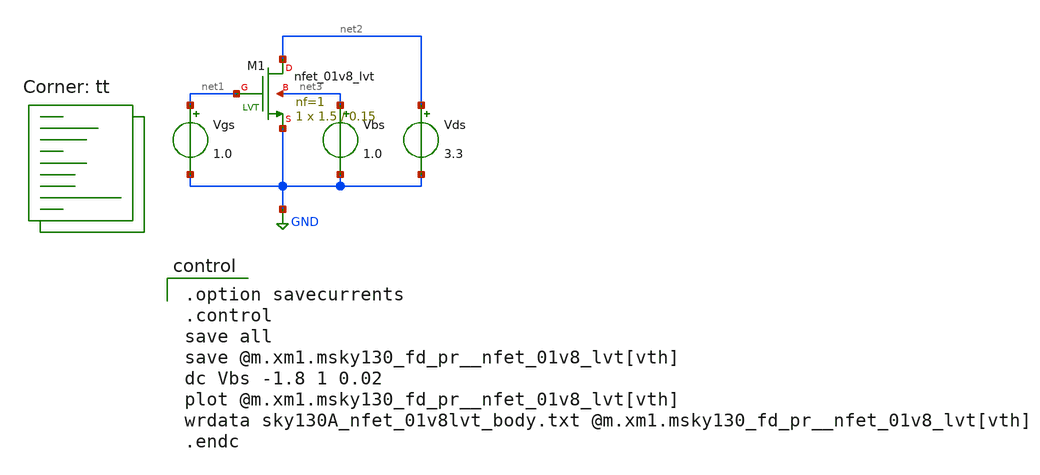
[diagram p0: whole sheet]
** sch_path: xschem/MOSFET/sky130A_nfet_01v8lvt_body.sch
**.subckt sky130A_nfet_01v8lvt_body
Vgs net1 GND 1.0
Vds net2 GND 3.3
Vbs net3 GND 1.0
XM1 net2 net1 GND net3 sky130_fd_pr__nfet_01v8_lvt L=0.15 W=1.5 nf=1 ad='int((1 + 1)/2) * 1.5 / 1 * 0.29'
+ as='int((1 + 2)/2) * 1.5 / 1 * 0.29' pd='2*int((1 + 1)/2) * (1.5 / 1 + 0.29)' ps='2*int((1 + 2)/2) * (1.5 / 1 + 0.29)'
+ nrd='0.29 / 1.5 ' nrs='0.29 / 1.5 ' sa=0 sb=0 sd=0 mult=1 m=1
**** begin user architecture code

.option savecurrents
.control
save all
save @m.xm1.msky130_fd_pr__nfet_01v8_lvt[vth]
dc Vbs -1.8 1 0.02
plot @m.xm1.msky130_fd_pr__nfet_01v8_lvt[vth]
wrdata sky130A_nfet_01v8lvt_body.txt @m.xm1.msky130_fd_pr__nfet_01v8_lvt[vth]
.endc

.lib $::SKYWATER_MODELS/sky130.lib.spice tt
**** end user architecture code
**.ends
.GLOBAL GND
.end
